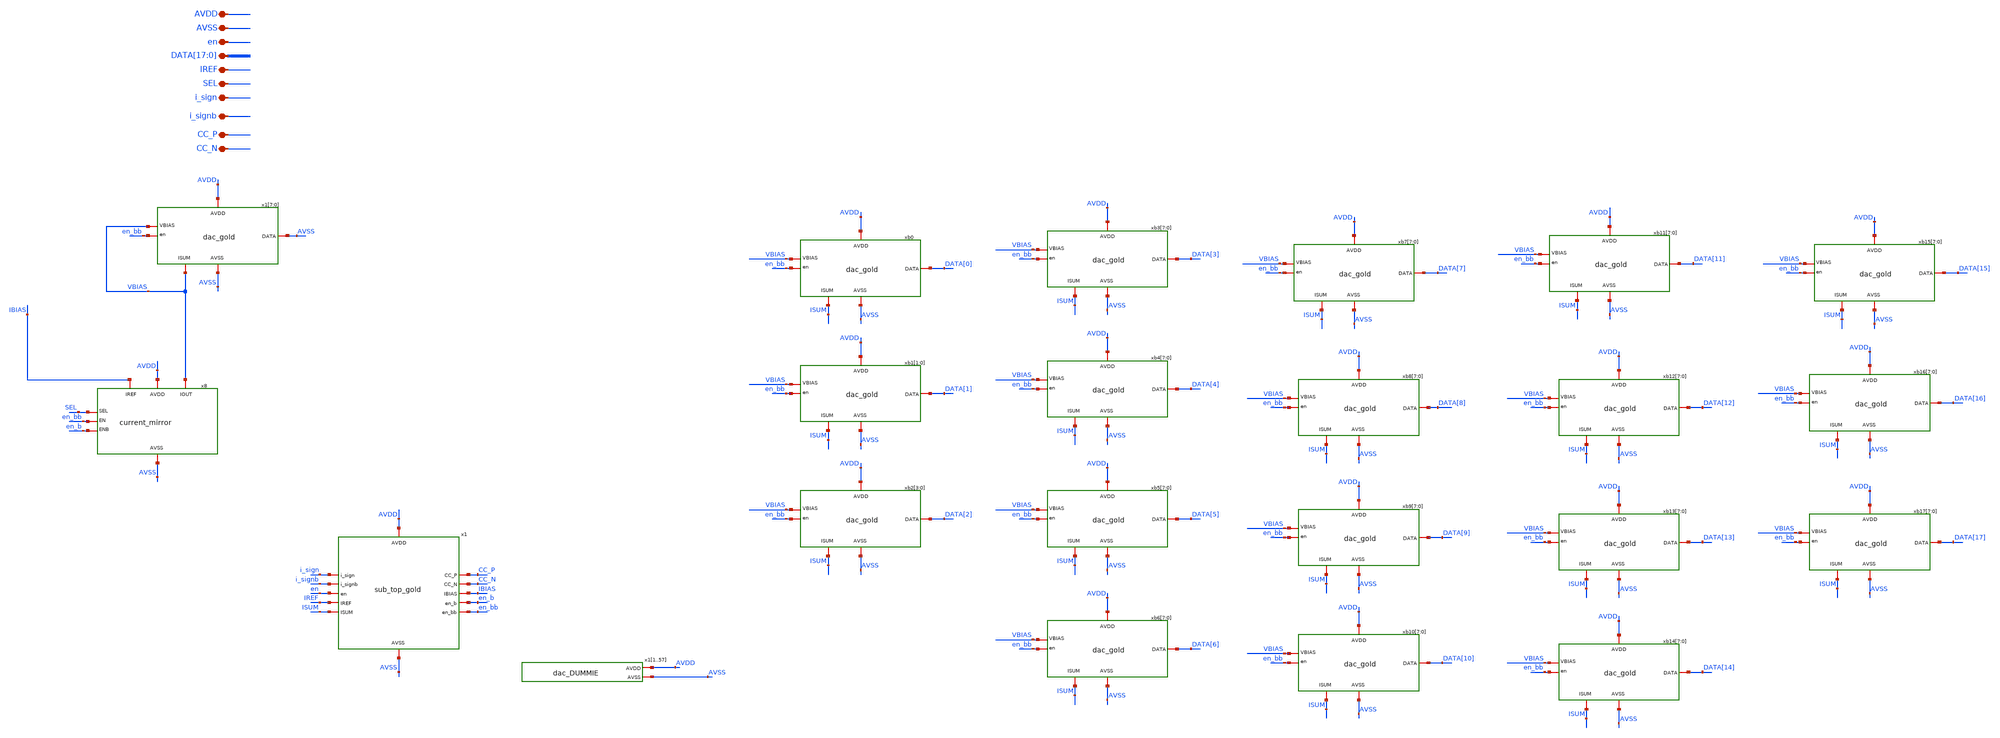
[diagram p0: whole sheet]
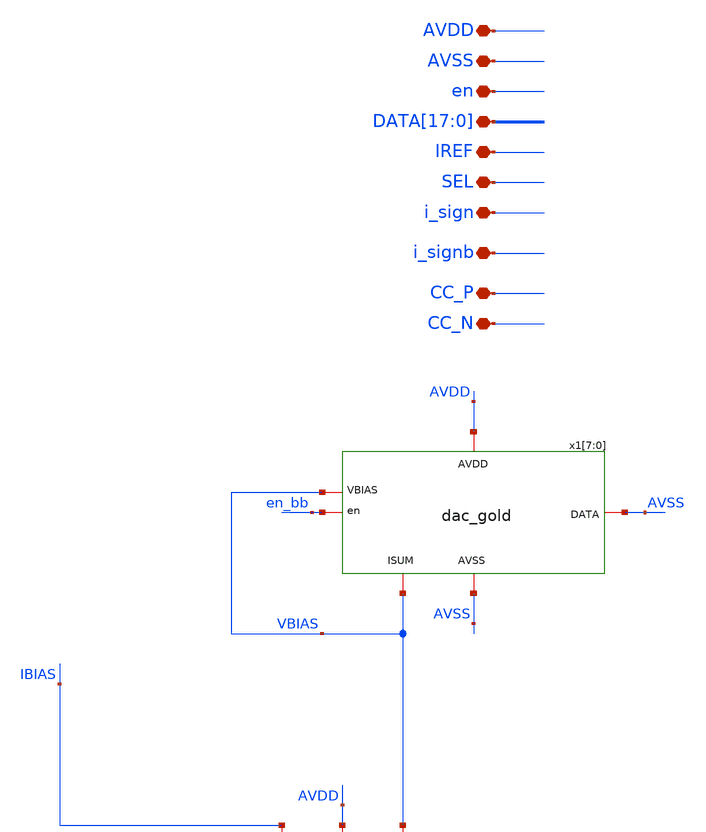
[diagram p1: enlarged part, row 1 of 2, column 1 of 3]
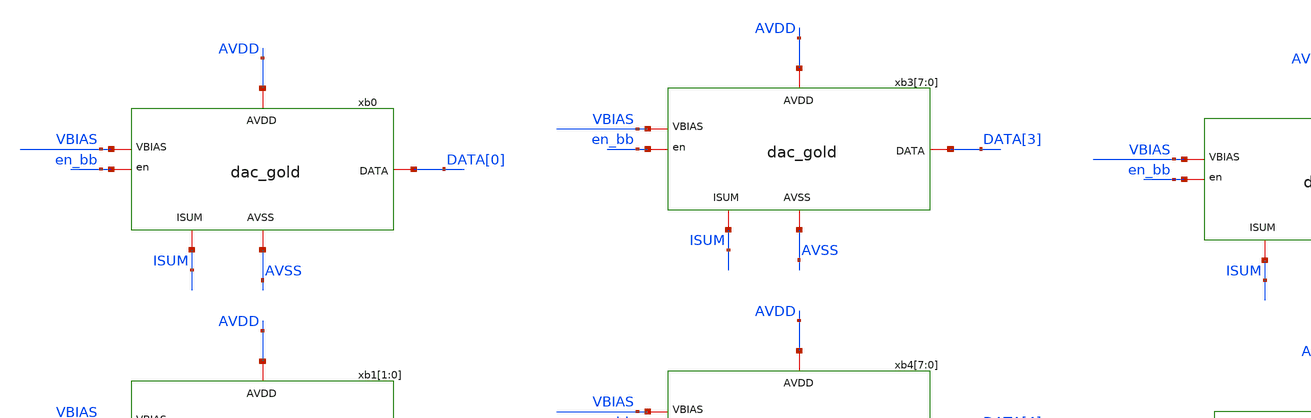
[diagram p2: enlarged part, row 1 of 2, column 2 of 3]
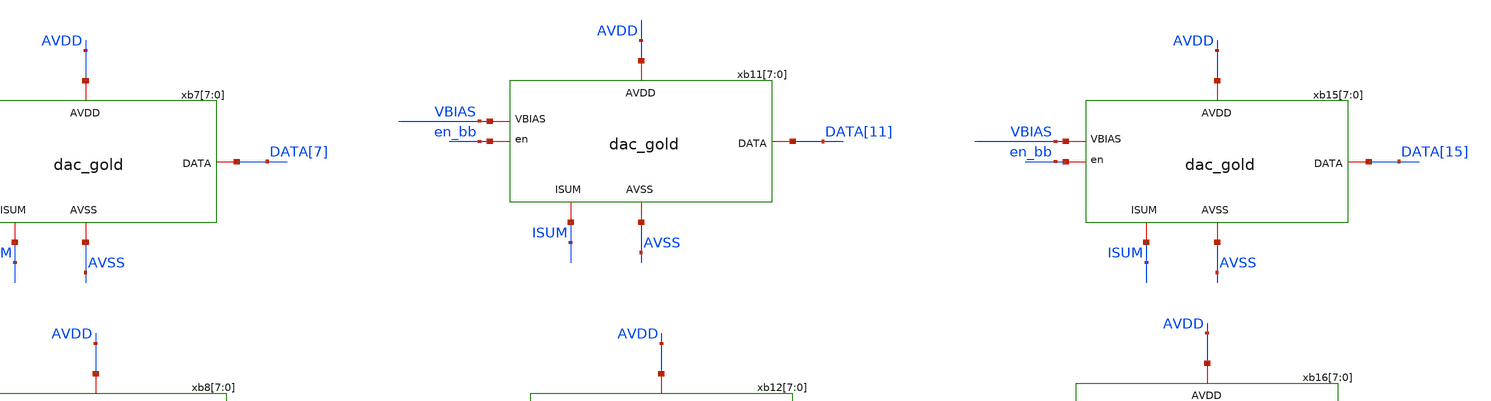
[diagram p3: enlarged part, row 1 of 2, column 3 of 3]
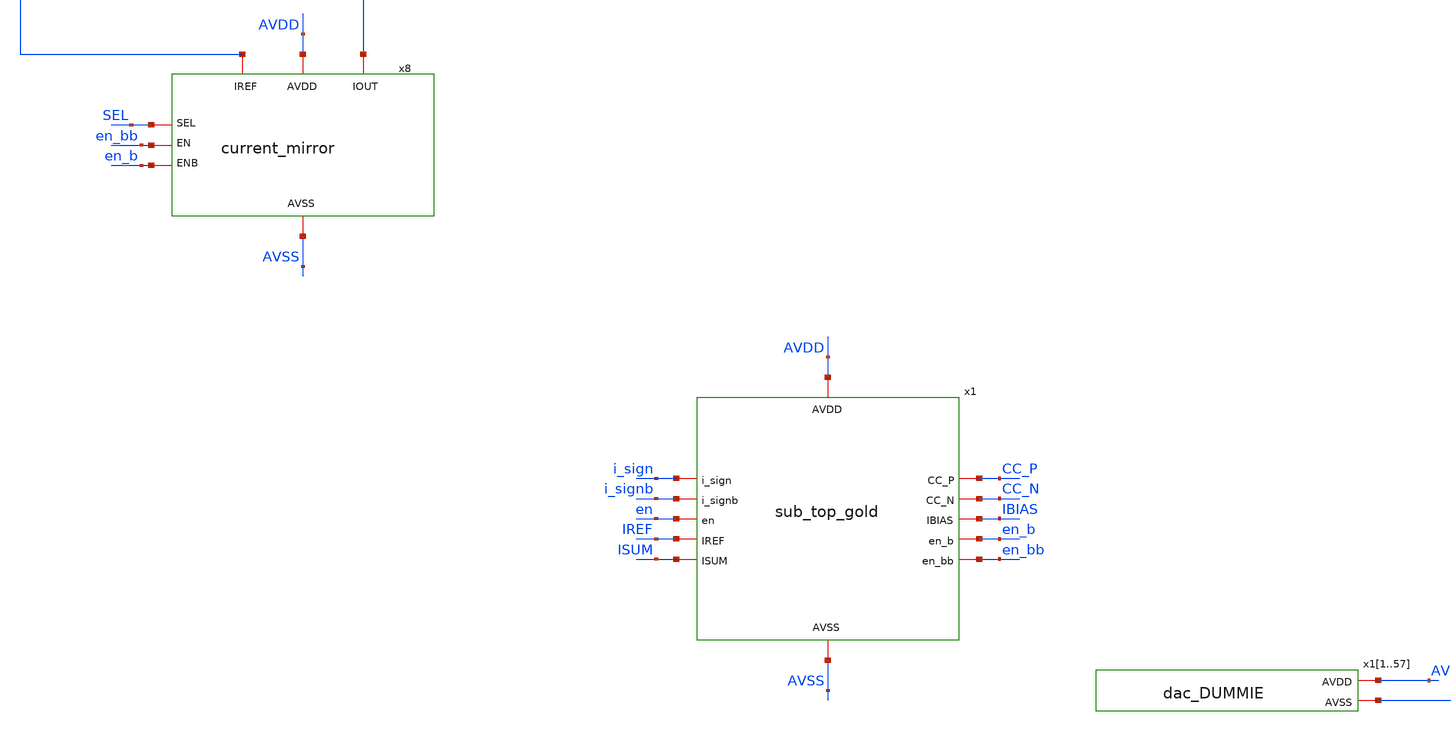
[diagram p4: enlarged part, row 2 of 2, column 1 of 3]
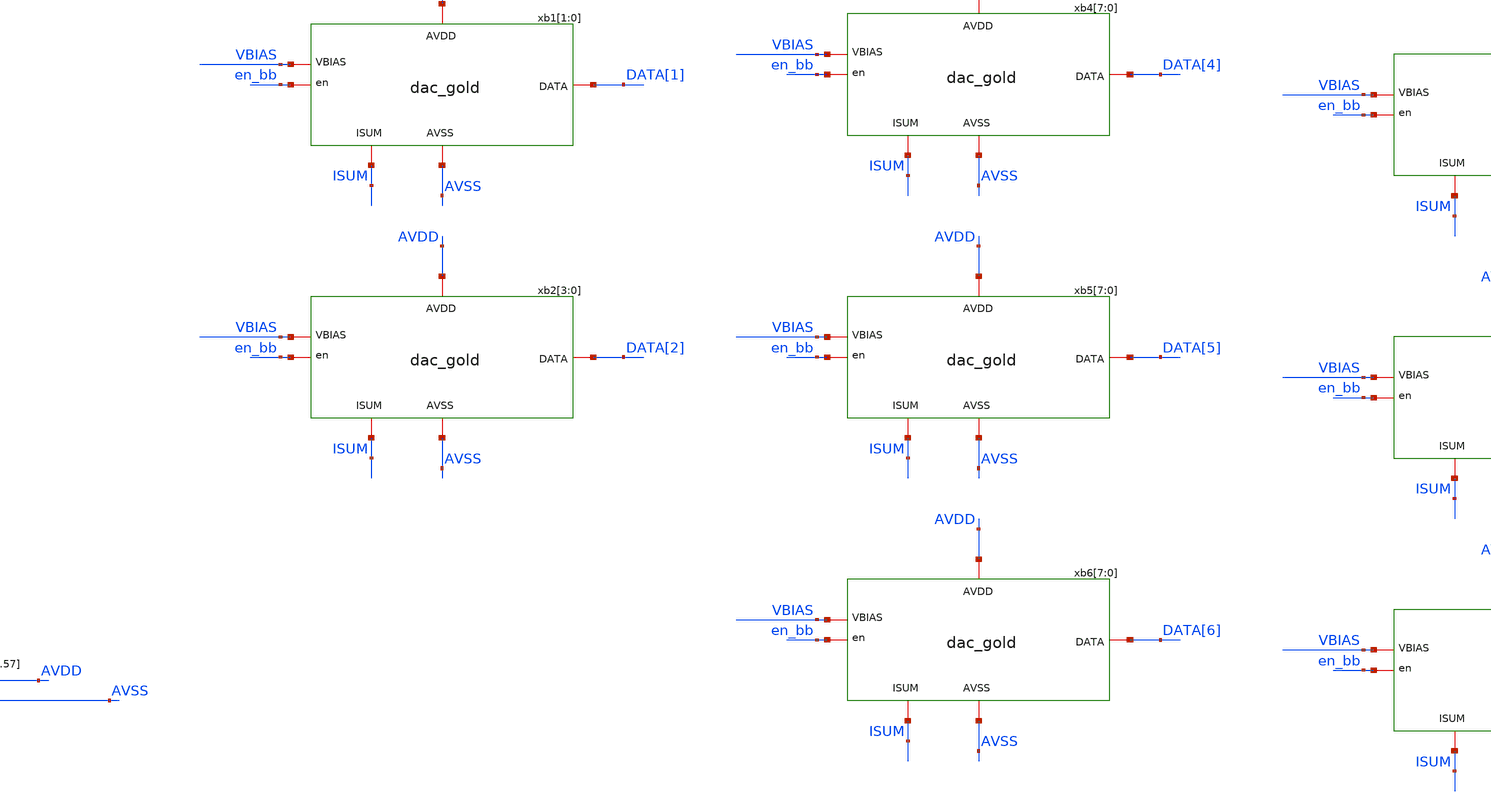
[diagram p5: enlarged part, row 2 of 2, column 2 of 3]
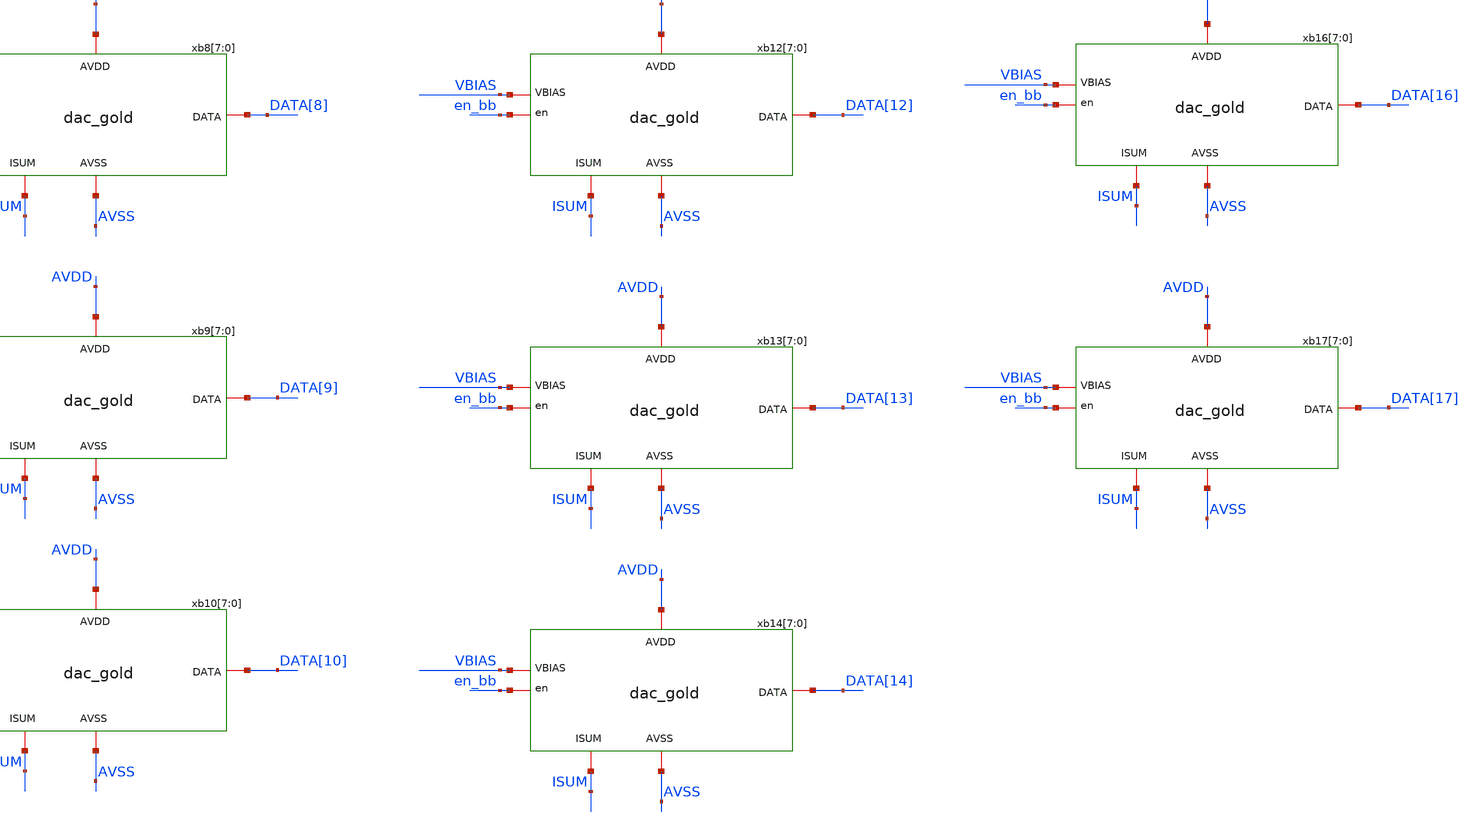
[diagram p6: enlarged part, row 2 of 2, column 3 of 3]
** sch_path: current_generator/analog/DAC/schematics/dac_top_gold.sch
**.subckt dac_top_gold AVDD AVSS en
*+ DATA[17],DATA[16],DATA[15],DATA[14],DATA[13],DATA[12],DATA[11],DATA[10],DATA[9],DATA[8],DATA[7],DATA[6],DATA[5],DATA[4],DATA[3],DATA[2],DATA[1],DATA[0] IREF SEL i_sign CC_P CC_N i_signb
*.iopin AVDD
*.iopin AVSS
*.iopin en
*.iopin
*+ DATA[17],DATA[16],DATA[15],DATA[14],DATA[13],DATA[12],DATA[11],DATA[10],DATA[9],DATA[8],DATA[7],DATA[6],DATA[5],DATA[4],DATA[3],DATA[2],DATA[1],DATA[0]
*.iopin IREF
*.iopin SEL
*.iopin i_sign
*.iopin CC_P
*.iopin CC_N
*.iopin i_signb
x8 AVDD AVSS en_bb en_b SEL IBIAS VBIAS current_mirror
xb0 AVDD AVSS VBIAS en_bb DATA[0] ISUM dac_gold
xb1[1] AVDD AVSS VBIAS en_bb DATA[1] ISUM dac_gold
xb1[0] AVDD AVSS VBIAS en_bb DATA[1] ISUM dac_gold
xb2[3] AVDD AVSS VBIAS en_bb DATA[2] ISUM dac_gold
xb2[2] AVDD AVSS VBIAS en_bb DATA[2] ISUM dac_gold
xb2[1] AVDD AVSS VBIAS en_bb DATA[2] ISUM dac_gold
xb2[0] AVDD AVSS VBIAS en_bb DATA[2] ISUM dac_gold
xb3[7] AVDD AVSS VBIAS en_bb DATA[3] ISUM dac_gold
xb3[6] AVDD AVSS VBIAS en_bb DATA[3] ISUM dac_gold
xb3[5] AVDD AVSS VBIAS en_bb DATA[3] ISUM dac_gold
xb3[4] AVDD AVSS VBIAS en_bb DATA[3] ISUM dac_gold
xb3[3] AVDD AVSS VBIAS en_bb DATA[3] ISUM dac_gold
xb3[2] AVDD AVSS VBIAS en_bb DATA[3] ISUM dac_gold
xb3[1] AVDD AVSS VBIAS en_bb DATA[3] ISUM dac_gold
xb3[0] AVDD AVSS VBIAS en_bb DATA[3] ISUM dac_gold
xb4[7] AVDD AVSS VBIAS en_bb DATA[4] ISUM dac_gold
xb4[6] AVDD AVSS VBIAS en_bb DATA[4] ISUM dac_gold
xb4[5] AVDD AVSS VBIAS en_bb DATA[4] ISUM dac_gold
xb4[4] AVDD AVSS VBIAS en_bb DATA[4] ISUM dac_gold
xb4[3] AVDD AVSS VBIAS en_bb DATA[4] ISUM dac_gold
xb4[2] AVDD AVSS VBIAS en_bb DATA[4] ISUM dac_gold
xb4[1] AVDD AVSS VBIAS en_bb DATA[4] ISUM dac_gold
xb4[0] AVDD AVSS VBIAS en_bb DATA[4] ISUM dac_gold
xb5[7] AVDD AVSS VBIAS en_bb DATA[5] ISUM dac_gold
xb5[6] AVDD AVSS VBIAS en_bb DATA[5] ISUM dac_gold
xb5[5] AVDD AVSS VBIAS en_bb DATA[5] ISUM dac_gold
xb5[4] AVDD AVSS VBIAS en_bb DATA[5] ISUM dac_gold
xb5[3] AVDD AVSS VBIAS en_bb DATA[5] ISUM dac_gold
xb5[2] AVDD AVSS VBIAS en_bb DATA[5] ISUM dac_gold
xb5[1] AVDD AVSS VBIAS en_bb DATA[5] ISUM dac_gold
xb5[0] AVDD AVSS VBIAS en_bb DATA[5] ISUM dac_gold
xb6[7] AVDD AVSS VBIAS en_bb DATA[6] ISUM dac_gold
xb6[6] AVDD AVSS VBIAS en_bb DATA[6] ISUM dac_gold
xb6[5] AVDD AVSS VBIAS en_bb DATA[6] ISUM dac_gold
xb6[4] AVDD AVSS VBIAS en_bb DATA[6] ISUM dac_gold
xb6[3] AVDD AVSS VBIAS en_bb DATA[6] ISUM dac_gold
xb6[2] AVDD AVSS VBIAS en_bb DATA[6] ISUM dac_gold
xb6[1] AVDD AVSS VBIAS en_bb DATA[6] ISUM dac_gold
xb6[0] AVDD AVSS VBIAS en_bb DATA[6] ISUM dac_gold
xb7[7] AVDD AVSS VBIAS en_bb DATA[7] ISUM dac_gold
xb7[6] AVDD AVSS VBIAS en_bb DATA[7] ISUM dac_gold
xb7[5] AVDD AVSS VBIAS en_bb DATA[7] ISUM dac_gold
xb7[4] AVDD AVSS VBIAS en_bb DATA[7] ISUM dac_gold
xb7[3] AVDD AVSS VBIAS en_bb DATA[7] ISUM dac_gold
xb7[2] AVDD AVSS VBIAS en_bb DATA[7] ISUM dac_gold
xb7[1] AVDD AVSS VBIAS en_bb DATA[7] ISUM dac_gold
xb7[0] AVDD AVSS VBIAS en_bb DATA[7] ISUM dac_gold
xb8[7] AVDD AVSS VBIAS en_bb DATA[8] ISUM dac_gold
xb8[6] AVDD AVSS VBIAS en_bb DATA[8] ISUM dac_gold
xb8[5] AVDD AVSS VBIAS en_bb DATA[8] ISUM dac_gold
xb8[4] AVDD AVSS VBIAS en_bb DATA[8] ISUM dac_gold
xb8[3] AVDD AVSS VBIAS en_bb DATA[8] ISUM dac_gold
xb8[2] AVDD AVSS VBIAS en_bb DATA[8] ISUM dac_gold
xb8[1] AVDD AVSS VBIAS en_bb DATA[8] ISUM dac_gold
xb8[0] AVDD AVSS VBIAS en_bb DATA[8] ISUM dac_gold
xb9[7] AVDD AVSS VBIAS en_bb DATA[9] ISUM dac_gold
xb9[6] AVDD AVSS VBIAS en_bb DATA[9] ISUM dac_gold
xb9[5] AVDD AVSS VBIAS en_bb DATA[9] ISUM dac_gold
xb9[4] AVDD AVSS VBIAS en_bb DATA[9] ISUM dac_gold
xb9[3] AVDD AVSS VBIAS en_bb DATA[9] ISUM dac_gold
xb9[2] AVDD AVSS VBIAS en_bb DATA[9] ISUM dac_gold
xb9[1] AVDD AVSS VBIAS en_bb DATA[9] ISUM dac_gold
xb9[0] AVDD AVSS VBIAS en_bb DATA[9] ISUM dac_gold
xb10[7] AVDD AVSS VBIAS en_bb DATA[10] ISUM dac_gold
xb10[6] AVDD AVSS VBIAS en_bb DATA[10] ISUM dac_gold
xb10[5] AVDD AVSS VBIAS en_bb DATA[10] ISUM dac_gold
xb10[4] AVDD AVSS VBIAS en_bb DATA[10] ISUM dac_gold
xb10[3] AVDD AVSS VBIAS en_bb DATA[10] ISUM dac_gold
xb10[2] AVDD AVSS VBIAS en_bb DATA[10] ISUM dac_gold
xb10[1] AVDD AVSS VBIAS en_bb DATA[10] ISUM dac_gold
xb10[0] AVDD AVSS VBIAS en_bb DATA[10] ISUM dac_gold
xb11[7] AVDD AVSS VBIAS en_bb DATA[11] ISUM dac_gold
xb11[6] AVDD AVSS VBIAS en_bb DATA[11] ISUM dac_gold
xb11[5] AVDD AVSS VBIAS en_bb DATA[11] ISUM dac_gold
xb11[4] AVDD AVSS VBIAS en_bb DATA[11] ISUM dac_gold
xb11[3] AVDD AVSS VBIAS en_bb DATA[11] ISUM dac_gold
xb11[2] AVDD AVSS VBIAS en_bb DATA[11] ISUM dac_gold
xb11[1] AVDD AVSS VBIAS en_bb DATA[11] ISUM dac_gold
xb11[0] AVDD AVSS VBIAS en_bb DATA[11] ISUM dac_gold
xb12[7] AVDD AVSS VBIAS en_bb DATA[12] ISUM dac_gold
xb12[6] AVDD AVSS VBIAS en_bb DATA[12] ISUM dac_gold
xb12[5] AVDD AVSS VBIAS en_bb DATA[12] ISUM dac_gold
xb12[4] AVDD AVSS VBIAS en_bb DATA[12] ISUM dac_gold
xb12[3] AVDD AVSS VBIAS en_bb DATA[12] ISUM dac_gold
xb12[2] AVDD AVSS VBIAS en_bb DATA[12] ISUM dac_gold
xb12[1] AVDD AVSS VBIAS en_bb DATA[12] ISUM dac_gold
xb12[0] AVDD AVSS VBIAS en_bb DATA[12] ISUM dac_gold
xb13[7] AVDD AVSS VBIAS en_bb DATA[13] ISUM dac_gold
xb13[6] AVDD AVSS VBIAS en_bb DATA[13] ISUM dac_gold
xb13[5] AVDD AVSS VBIAS en_bb DATA[13] ISUM dac_gold
xb13[4] AVDD AVSS VBIAS en_bb DATA[13] ISUM dac_gold
xb13[3] AVDD AVSS VBIAS en_bb DATA[13] ISUM dac_gold
xb13[2] AVDD AVSS VBIAS en_bb DATA[13] ISUM dac_gold
xb13[1] AVDD AVSS VBIAS en_bb DATA[13] ISUM dac_gold
xb13[0] AVDD AVSS VBIAS en_bb DATA[13] ISUM dac_gold
xb14[7] AVDD AVSS VBIAS en_bb DATA[14] ISUM dac_gold
xb14[6] AVDD AVSS VBIAS en_bb DATA[14] ISUM dac_gold
xb14[5] AVDD AVSS VBIAS en_bb DATA[14] ISUM dac_gold
xb14[4] AVDD AVSS VBIAS en_bb DATA[14] ISUM dac_gold
xb14[3] AVDD AVSS VBIAS en_bb DATA[14] ISUM dac_gold
xb14[2] AVDD AVSS VBIAS en_bb DATA[14] ISUM dac_gold
xb14[1] AVDD AVSS VBIAS en_bb DATA[14] ISUM dac_gold
xb14[0] AVDD AVSS VBIAS en_bb DATA[14] ISUM dac_gold
xb15[7] AVDD AVSS VBIAS en_bb DATA[15] ISUM dac_gold
xb15[6] AVDD AVSS VBIAS en_bb DATA[15] ISUM dac_gold
xb15[5] AVDD AVSS VBIAS en_bb DATA[15] ISUM dac_gold
xb15[4] AVDD AVSS VBIAS en_bb DATA[15] ISUM dac_gold
xb15[3] AVDD AVSS VBIAS en_bb DATA[15] ISUM dac_gold
xb15[2] AVDD AVSS VBIAS en_bb DATA[15] ISUM dac_gold
xb15[1] AVDD AVSS VBIAS en_bb DATA[15] ISUM dac_gold
xb15[0] AVDD AVSS VBIAS en_bb DATA[15] ISUM dac_gold
xb16[7] AVDD AVSS VBIAS en_bb DATA[16] ISUM dac_gold
xb16[6] AVDD AVSS VBIAS en_bb DATA[16] ISUM dac_gold
xb16[5] AVDD AVSS VBIAS en_bb DATA[16] ISUM dac_gold
xb16[4] AVDD AVSS VBIAS en_bb DATA[16] ISUM dac_gold
xb16[3] AVDD AVSS VBIAS en_bb DATA[16] ISUM dac_gold
xb16[2] AVDD AVSS VBIAS en_bb DATA[16] ISUM dac_gold
xb16[1] AVDD AVSS VBIAS en_bb DATA[16] ISUM dac_gold
xb16[0] AVDD AVSS VBIAS en_bb DATA[16] ISUM dac_gold
xb17[7] AVDD AVSS VBIAS en_bb DATA[17] ISUM dac_gold
xb17[6] AVDD AVSS VBIAS en_bb DATA[17] ISUM dac_gold
xb17[5] AVDD AVSS VBIAS en_bb DATA[17] ISUM dac_gold
xb17[4] AVDD AVSS VBIAS en_bb DATA[17] ISUM dac_gold
xb17[3] AVDD AVSS VBIAS en_bb DATA[17] ISUM dac_gold
xb17[2] AVDD AVSS VBIAS en_bb DATA[17] ISUM dac_gold
xb17[1] AVDD AVSS VBIAS en_bb DATA[17] ISUM dac_gold
xb17[0] AVDD AVSS VBIAS en_bb DATA[17] ISUM dac_gold
x1 AVDD CC_P en CC_N AVSS IREF i_sign IBIAS i_signb en_b ISUM en_bb sub_top_gold
x1[7] AVDD AVSS VBIAS en_bb AVSS VBIAS dac_gold
x1[6] AVDD AVSS VBIAS en_bb AVSS VBIAS dac_gold
x1[5] AVDD AVSS VBIAS en_bb AVSS VBIAS dac_gold
x1[4] AVDD AVSS VBIAS en_bb AVSS VBIAS dac_gold
x1[3] AVDD AVSS VBIAS en_bb AVSS VBIAS dac_gold
x1[2] AVDD AVSS VBIAS en_bb AVSS VBIAS dac_gold
x1[1] AVDD AVSS VBIAS en_bb AVSS VBIAS dac_gold
x1[0] AVDD AVSS VBIAS en_bb AVSS VBIAS dac_gold
x11 AVDD AVSS dac_DUMMIE
x12 AVDD AVSS dac_DUMMIE
x13 AVDD AVSS dac_DUMMIE
x14 AVDD AVSS dac_DUMMIE
x15 AVDD AVSS dac_DUMMIE
x16 AVDD AVSS dac_DUMMIE
x17 AVDD AVSS dac_DUMMIE
x18 AVDD AVSS dac_DUMMIE
x19 AVDD AVSS dac_DUMMIE
x110 AVDD AVSS dac_DUMMIE
x111 AVDD AVSS dac_DUMMIE
x112 AVDD AVSS dac_DUMMIE
x113 AVDD AVSS dac_DUMMIE
x114 AVDD AVSS dac_DUMMIE
x115 AVDD AVSS dac_DUMMIE
x116 AVDD AVSS dac_DUMMIE
x117 AVDD AVSS dac_DUMMIE
x118 AVDD AVSS dac_DUMMIE
x119 AVDD AVSS dac_DUMMIE
x120 AVDD AVSS dac_DUMMIE
x121 AVDD AVSS dac_DUMMIE
x122 AVDD AVSS dac_DUMMIE
x123 AVDD AVSS dac_DUMMIE
x124 AVDD AVSS dac_DUMMIE
x125 AVDD AVSS dac_DUMMIE
x126 AVDD AVSS dac_DUMMIE
x127 AVDD AVSS dac_DUMMIE
x128 AVDD AVSS dac_DUMMIE
x129 AVDD AVSS dac_DUMMIE
x130 AVDD AVSS dac_DUMMIE
x131 AVDD AVSS dac_DUMMIE
x132 AVDD AVSS dac_DUMMIE
x133 AVDD AVSS dac_DUMMIE
x134 AVDD AVSS dac_DUMMIE
x135 AVDD AVSS dac_DUMMIE
x136 AVDD AVSS dac_DUMMIE
x137 AVDD AVSS dac_DUMMIE
x138 AVDD AVSS dac_DUMMIE
x139 AVDD AVSS dac_DUMMIE
x140 AVDD AVSS dac_DUMMIE
x141 AVDD AVSS dac_DUMMIE
x142 AVDD AVSS dac_DUMMIE
x143 AVDD AVSS dac_DUMMIE
x144 AVDD AVSS dac_DUMMIE
x145 AVDD AVSS dac_DUMMIE
x146 AVDD AVSS dac_DUMMIE
x147 AVDD AVSS dac_DUMMIE
x148 AVDD AVSS dac_DUMMIE
x149 AVDD AVSS dac_DUMMIE
x150 AVDD AVSS dac_DUMMIE
x151 AVDD AVSS dac_DUMMIE
x152 AVDD AVSS dac_DUMMIE
x153 AVDD AVSS dac_DUMMIE
x154 AVDD AVSS dac_DUMMIE
x155 AVDD AVSS dac_DUMMIE
x156 AVDD AVSS dac_DUMMIE
x157 AVDD AVSS dac_DUMMIE
**.ends
.end
